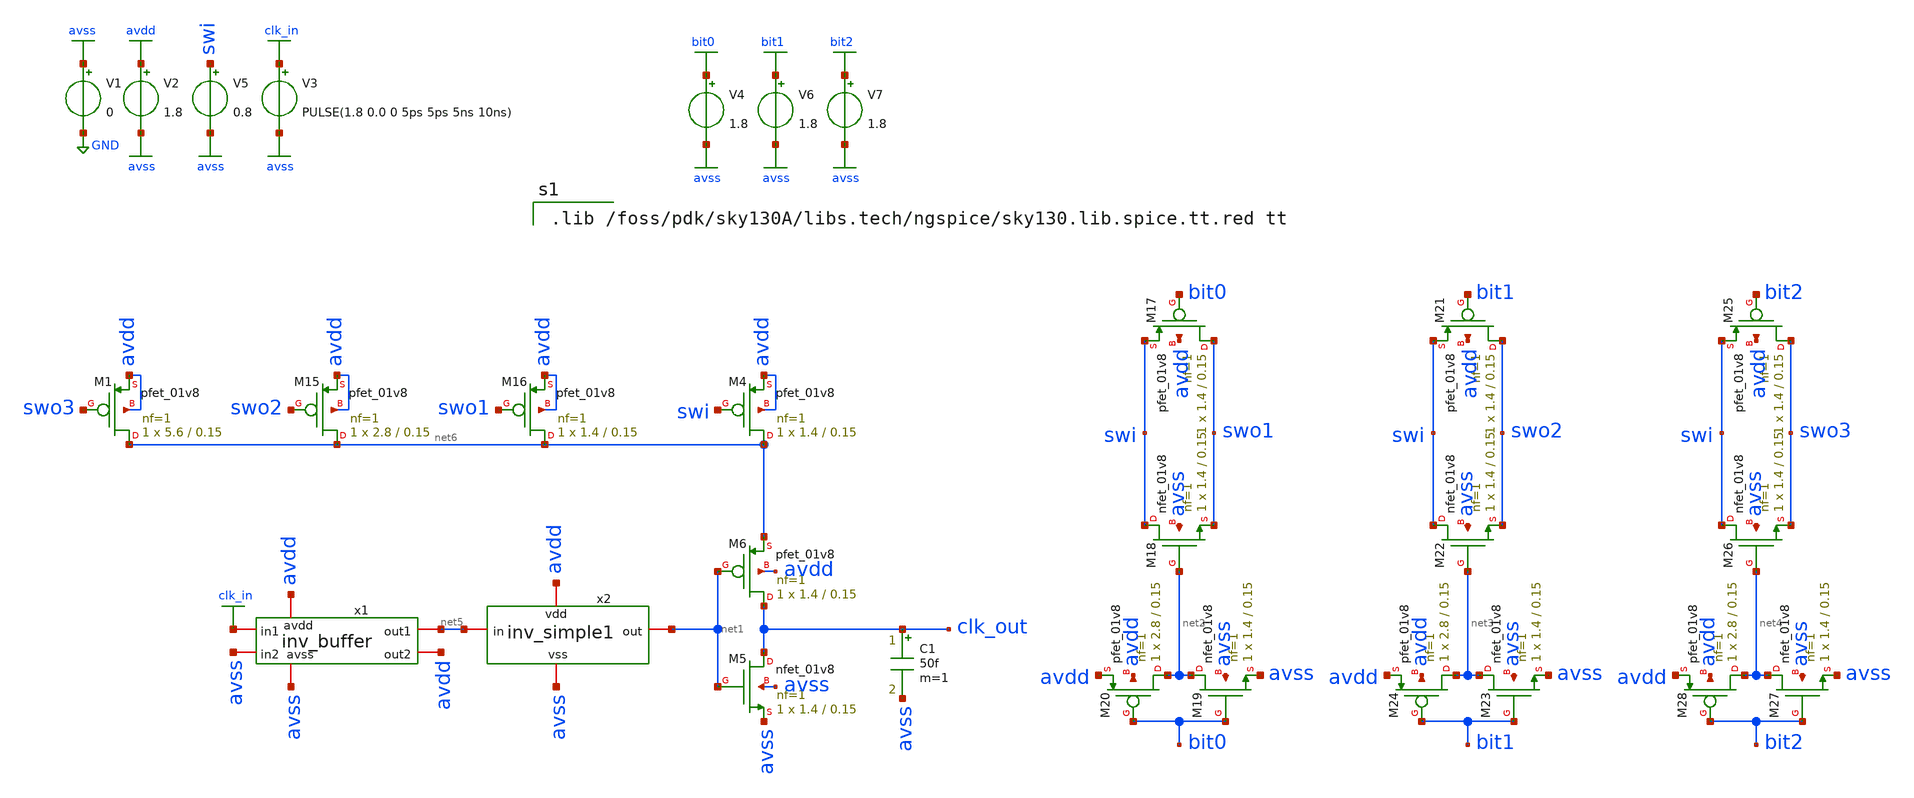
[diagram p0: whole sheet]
** sch_path: xschem/slopebuf_sim3.sch
**.subckt slopebuf_sim3
V1 avss GND 0
V2 avdd avss 1.8
V3 clk_in avss PULSE(1.8 0.0 0 5ps 5ps 5ns 10ns)
V5 swi avss 0.8
XM5 clk_out net1 avss avss sky130_fd_pr__nfet_01v8 L=0.15 W=1.4 nf=1 ad='int((nf+1)/2) * W/nf * 0.29'
+ as='int((nf+2)/2) * W/nf * 0.29' pd='2*int((nf+1)/2) * (W/nf + 0.29)' ps='2*int((nf+2)/2) * (W/nf + 0.29)'
+ nrd='0.29 / W' nrs='0.29 / W' sa=0 sb=0 sd=0 mult=1 m=1
XM6 clk_out net1 net6 avdd sky130_fd_pr__pfet_01v8 L=0.15 W=1.4 nf=1 ad='int((nf+1)/2) * W/nf * 0.29'
+ as='int((nf+2)/2) * W/nf * 0.29' pd='2*int((nf+1)/2) * (W/nf + 0.29)' ps='2*int((nf+2)/2) * (W/nf + 0.29)'
+ nrd='0.29 / W' nrs='0.29 / W' sa=0 sb=0 sd=0 mult=1 m=1
XM4 net6 swi avdd avdd sky130_fd_pr__pfet_01v8 L=0.15 W=1.4 nf=1 ad='int((nf+1)/2) * W/nf * 0.29' as='int((nf+2)/2) * W/nf * 0.29'
+ pd='2*int((nf+1)/2) * (W/nf + 0.29)' ps='2*int((nf+2)/2) * (W/nf + 0.29)' nrd='0.29 / W' nrs='0.29 / W'
+ sa=0 sb=0 sd=0 mult=1 m=1
C1 clk_out avss 50f m=1
XM1 net6 swo3 avdd avdd sky130_fd_pr__pfet_01v8 L=0.15 W=5.6 nf=1 ad='int((nf+1)/2) * W/nf * 0.29' as='int((nf+2)/2) * W/nf * 0.29'
+ pd='2*int((nf+1)/2) * (W/nf + 0.29)' ps='2*int((nf+2)/2) * (W/nf + 0.29)' nrd='0.29 / W' nrs='0.29 / W'
+ sa=0 sb=0 sd=0 mult=1 m=1
XM15 net6 swo2 avdd avdd sky130_fd_pr__pfet_01v8 L=0.15 W=2.8 nf=1 ad='int((nf+1)/2) * W/nf * 0.29' as='int((nf+2)/2) * W/nf * 0.29'
+ pd='2*int((nf+1)/2) * (W/nf + 0.29)' ps='2*int((nf+2)/2) * (W/nf + 0.29)' nrd='0.29 / W' nrs='0.29 / W'
+ sa=0 sb=0 sd=0 mult=1 m=1
XM16 net6 swo1 avdd avdd sky130_fd_pr__pfet_01v8 L=0.15 W=1.4 nf=1 ad='int((nf+1)/2) * W/nf * 0.29' as='int((nf+2)/2) * W/nf * 0.29'
+ pd='2*int((nf+1)/2) * (W/nf + 0.29)' ps='2*int((nf+2)/2) * (W/nf + 0.29)' nrd='0.29 / W' nrs='0.29 / W'
+ sa=0 sb=0 sd=0 mult=1 m=1
XM17 swo1 bit0 swi avdd sky130_fd_pr__pfet_01v8 L=0.15 W=1.4 nf=1 ad='int((nf+1)/2) * W/nf * 0.29' as='int((nf+2)/2) * W/nf * 0.29'
+ pd='2*int((nf+1)/2) * (W/nf + 0.29)' ps='2*int((nf+2)/2) * (W/nf + 0.29)' nrd='0.29 / W' nrs='0.29 / W'
+ sa=0 sb=0 sd=0 mult=1 m=1
XM18 swi net2 swo1 avss sky130_fd_pr__nfet_01v8 L=0.15 W=1.4 nf=1 ad='int((nf+1)/2) * W/nf * 0.29' as='int((nf+2)/2) * W/nf * 0.29'
+ pd='2*int((nf+1)/2) * (W/nf + 0.29)' ps='2*int((nf+2)/2) * (W/nf + 0.29)' nrd='0.29 / W' nrs='0.29 / W'
+ sa=0 sb=0 sd=0 mult=1 m=1
XM19 net2 bit0 avss avss sky130_fd_pr__nfet_01v8 L=0.15 W=1.4 nf=1 ad='int((nf+1)/2) * W/nf * 0.29' as='int((nf+2)/2) * W/nf * 0.29'
+ pd='2*int((nf+1)/2) * (W/nf + 0.29)' ps='2*int((nf+2)/2) * (W/nf + 0.29)' nrd='0.29 / W' nrs='0.29 / W'
+ sa=0 sb=0 sd=0 mult=1 m=1
XM20 net2 bit0 avdd avdd sky130_fd_pr__pfet_01v8 L=0.15 W=2.8 nf=1 ad='int((nf+1)/2) * W/nf * 0.29' as='int((nf+2)/2) * W/nf * 0.29'
+ pd='2*int((nf+1)/2) * (W/nf + 0.29)' ps='2*int((nf+2)/2) * (W/nf + 0.29)' nrd='0.29 / W' nrs='0.29 / W'
+ sa=0 sb=0 sd=0 mult=1 m=1
XM21 swo2 bit1 swi avdd sky130_fd_pr__pfet_01v8 L=0.15 W=1.4 nf=1 ad='int((nf+1)/2) * W/nf * 0.29' as='int((nf+2)/2) * W/nf * 0.29'
+ pd='2*int((nf+1)/2) * (W/nf + 0.29)' ps='2*int((nf+2)/2) * (W/nf + 0.29)' nrd='0.29 / W' nrs='0.29 / W'
+ sa=0 sb=0 sd=0 mult=1 m=1
XM22 swi net3 swo2 avss sky130_fd_pr__nfet_01v8 L=0.15 W=1.4 nf=1 ad='int((nf+1)/2) * W/nf * 0.29' as='int((nf+2)/2) * W/nf * 0.29'
+ pd='2*int((nf+1)/2) * (W/nf + 0.29)' ps='2*int((nf+2)/2) * (W/nf + 0.29)' nrd='0.29 / W' nrs='0.29 / W'
+ sa=0 sb=0 sd=0 mult=1 m=1
XM23 net3 bit1 avss avss sky130_fd_pr__nfet_01v8 L=0.15 W=1.4 nf=1 ad='int((nf+1)/2) * W/nf * 0.29' as='int((nf+2)/2) * W/nf * 0.29'
+ pd='2*int((nf+1)/2) * (W/nf + 0.29)' ps='2*int((nf+2)/2) * (W/nf + 0.29)' nrd='0.29 / W' nrs='0.29 / W'
+ sa=0 sb=0 sd=0 mult=1 m=1
XM24 net3 bit1 avdd avdd sky130_fd_pr__pfet_01v8 L=0.15 W=2.8 nf=1 ad='int((nf+1)/2) * W/nf * 0.29' as='int((nf+2)/2) * W/nf * 0.29'
+ pd='2*int((nf+1)/2) * (W/nf + 0.29)' ps='2*int((nf+2)/2) * (W/nf + 0.29)' nrd='0.29 / W' nrs='0.29 / W'
+ sa=0 sb=0 sd=0 mult=1 m=1
XM25 swo3 bit2 swi avdd sky130_fd_pr__pfet_01v8 L=0.15 W=1.4 nf=1 ad='int((nf+1)/2) * W/nf * 0.29' as='int((nf+2)/2) * W/nf * 0.29'
+ pd='2*int((nf+1)/2) * (W/nf + 0.29)' ps='2*int((nf+2)/2) * (W/nf + 0.29)' nrd='0.29 / W' nrs='0.29 / W'
+ sa=0 sb=0 sd=0 mult=1 m=1
XM26 swi net4 swo3 avss sky130_fd_pr__nfet_01v8 L=0.15 W=1.4 nf=1 ad='int((nf+1)/2) * W/nf * 0.29' as='int((nf+2)/2) * W/nf * 0.29'
+ pd='2*int((nf+1)/2) * (W/nf + 0.29)' ps='2*int((nf+2)/2) * (W/nf + 0.29)' nrd='0.29 / W' nrs='0.29 / W'
+ sa=0 sb=0 sd=0 mult=1 m=1
XM27 net4 bit2 avss avss sky130_fd_pr__nfet_01v8 L=0.15 W=1.4 nf=1 ad='int((nf+1)/2) * W/nf * 0.29' as='int((nf+2)/2) * W/nf * 0.29'
+ pd='2*int((nf+1)/2) * (W/nf + 0.29)' ps='2*int((nf+2)/2) * (W/nf + 0.29)' nrd='0.29 / W' nrs='0.29 / W'
+ sa=0 sb=0 sd=0 mult=1 m=1
XM28 net4 bit2 avdd avdd sky130_fd_pr__pfet_01v8 L=0.15 W=2.8 nf=1 ad='int((nf+1)/2) * W/nf * 0.29' as='int((nf+2)/2) * W/nf * 0.29'
+ pd='2*int((nf+1)/2) * (W/nf + 0.29)' ps='2*int((nf+2)/2) * (W/nf + 0.29)' nrd='0.29 / W' nrs='0.29 / W'
+ sa=0 sb=0 sd=0 mult=1 m=1
V4 bit0 avss 1.8
V6 bit1 avss 1.8
V7 bit2 avss 1.8
x1 avdd avss net5 avdd avss clk_in inv_buffer
x2 avdd net5 net1 avss inv_simple1
**** begin user architecture code

.lib /foss/pdk/sky130A/libs.tech/ngspice/sky130.lib.spice.tt.red tt



.control
save clk_in clk_out @V1[i] @V3[i]
alter v4 0
alter v6 0
alter v7 0
tran 0.05n 40n 20n
run
alter v4 1.8
alter v6 0
alter v7 0
tran 0.05n 40n 20n
run
alter v4 0
alter v6 1.8
alter v7 0
tran 0.05n 40n 20n
run
alter v4 1.8
alter v6 1.8
alter v7 0
tran 0.05n 40n 20n
run
alter v4 0
alter v6 0
alter v7 1.8
tran 0.05n 40n 20n
run
alter v4 1.8
alter v6 0
alter v7 1.8
tran 0.05n 40n 20n
run
alter v4 0
alter v6 1.8
alter v7 1.8
tran 0.05n 40n 20n
run
alter v4 1.8
alter v6 1.8
alter v7 1.8
tran 0.05n 40n 20n
run
plot tran1.clk_in tran1.clk_out tran2.clk_out tran3.clk_out tran4.clk_out tran5.clk_out
+ tran6.clk_out tran7.clk_out tran8.clk_out xlimit 24n 32n
*plot tran1.clk_in tran2.clk_in tran3.clk_in tran4.clk_in tran5.clk_in tran6.clk_in tran7.clk_in
*+ tran8.clk_in
plot tran1.@V1[i] tran5.@V1[i] tran8.@V1[i] tran1.@V3[i] tran5.@V3[i] tran8.@V3[i]
*plot tran1.clk_in tran1.s3 tran1.clk_out
.endc
.end


**** end user architecture code
**.ends
.GLOBAL avdd
.GLOBAL avss
.GLOBAL GND
.GLOBAL clk_in
.GLOBAL bit0
.GLOBAL bit1
.GLOBAL bit2
.end
